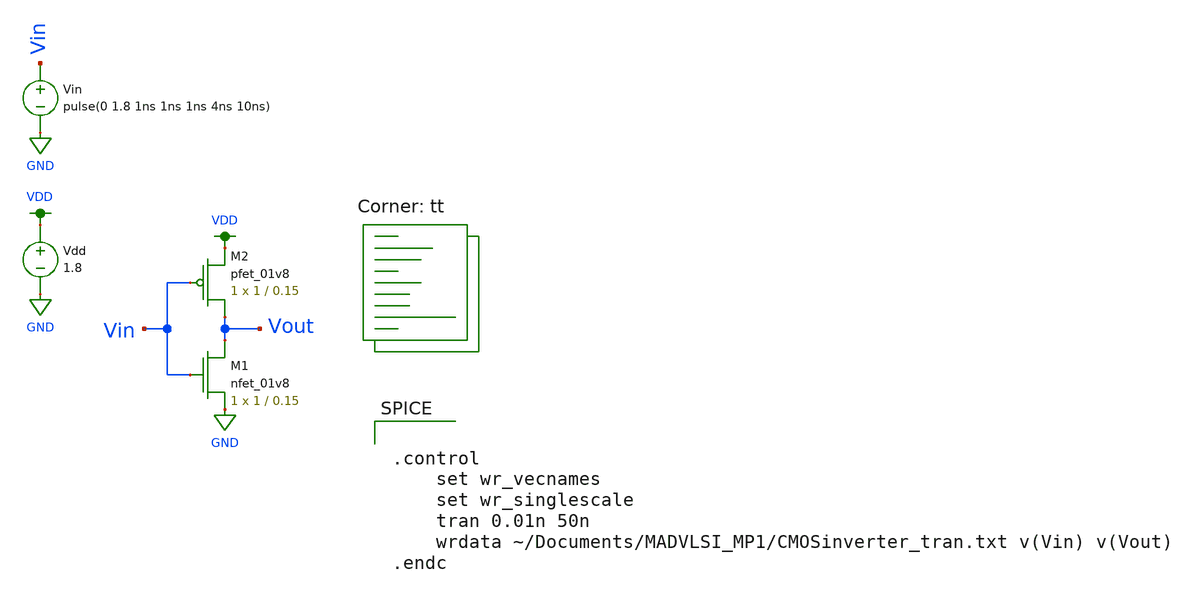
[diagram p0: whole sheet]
** sch_path: MADVLSI_MP1/CMOSinverter_tran.sch
**.subckt CMOSinverter_tran
XM1 Vout Vin GND GND sky130_fd_pr__nfet_01v8 L=0.15 W=1 nf=1 ad='int((nf+1)/2) * W/nf * 0.29' as='int((nf+2)/2) * W/nf * 0.29'
+ pd='2*int((nf+1)/2) * (W/nf + 0.29)' ps='2*int((nf+2)/2) * (W/nf + 0.29)' nrd='0.29 / W' nrs='0.29 / W'
+ sa=0 sb=0 sd=0 mult=1 m=1
Vdd VDD GND 1.8
XM2 Vout Vin VDD VDD sky130_fd_pr__pfet_01v8 L=0.15 W=1 nf=1 ad='int((nf+1)/2) * W/nf * 0.29' as='int((nf+2)/2) * W/nf * 0.29'
+ pd='2*int((nf+1)/2) * (W/nf + 0.29)' ps='2*int((nf+2)/2) * (W/nf + 0.29)' nrd='0.29 / W' nrs='0.29 / W'
+ sa=0 sb=0 sd=0 mult=1 m=1
Vin Vin GND pulse(0 1.8 1ns 1ns 1ns 4ns 10ns)
**** begin user architecture code


.control
	set wr_vecnames
	set wr_singlescale
	tran 0.01n 50n
	wrdata ~/Documents/MADVLSI_MP1/CMOSinverter_tran.txt v(Vin) v(Vout)
.endc

.lib $::SKYWATER_MODELS/sky130.lib.spice tt
**** end user architecture code
**.ends
.GLOBAL GND
.GLOBAL VDD
.end
